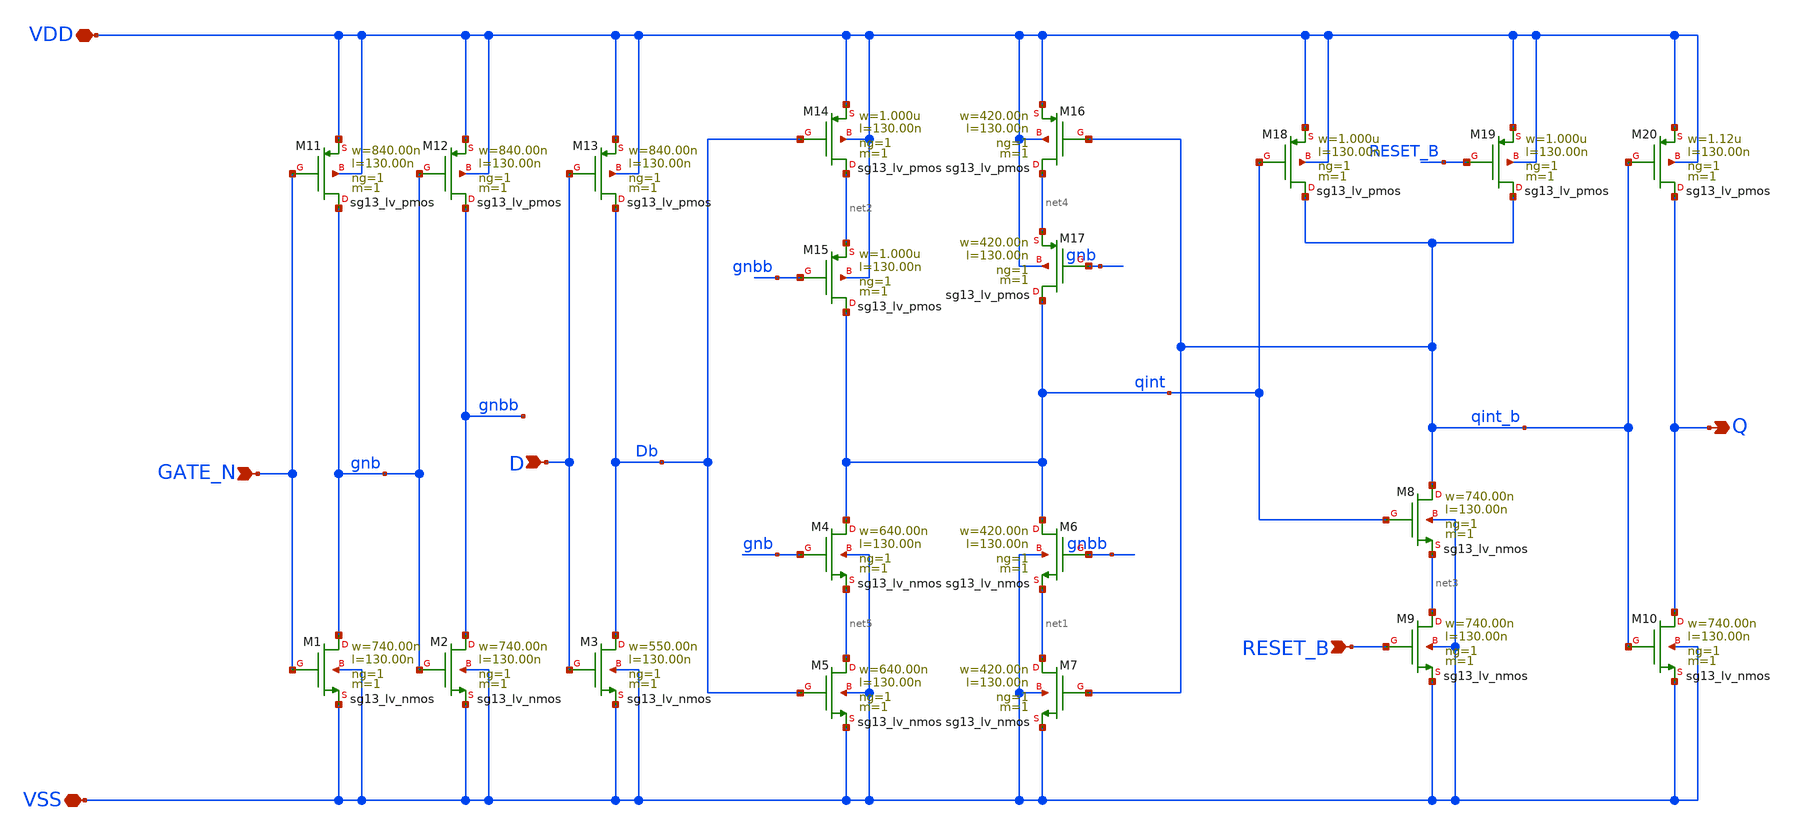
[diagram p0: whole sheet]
** sch_path: ihp-sg13g2/libs.tech/xschem/sg13g2_stdcells/sg13g2_dllrq_1.sch
* Copyright 2023 IHP PDK Authors
* Licensed under the Apache License, Version 2.0 (the "License");
* you may not use this file except in compliance with the License.
* You may obtain a copy of the License at
* https://www.apache.org/licenses/LICENSE-2.0
* Unless required by applicable law or agreed to in writing, software
* distributed under the License is distributed on an "AS IS" BASIS,
* WITHOUT WARRANTIES OR CONDITIONS OF ANY KIND, either express or implied.
* See the License for the specific language governing permissions and
* limitations under the License.
**.subckt sg13g2_dllrq_1 D GATE_N RESET_B Q VDD VSS
*.ipin D
*.ipin GATE_N
*.ipin RESET_B
*.opin Q
*.iopin VDD
*.iopin VSS
XM1 gnb GATE_N VSS VSS sg13_lv_nmos w=740.00n l=130.00n ng=1 m=1 mm_ok=1
XM2 gnbb gnb VSS VSS sg13_lv_nmos w=740.00n l=130.00n ng=1 m=1 mm_ok=1
XM3 Db D VSS VSS sg13_lv_nmos w=550.00n l=130.00n ng=1 m=1 mm_ok=1
XM4 qint gnb net5 VSS sg13_lv_nmos w=640.00n l=130.00n ng=1 m=1 mm_ok=1
XM5 net5 Db VSS VSS sg13_lv_nmos w=640.00n l=130.00n ng=1 m=1 mm_ok=1
XM6 qint gnbb net1 VSS sg13_lv_nmos w=420.00n l=130.00n ng=1 m=1 mm_ok=1
XM7 net1 qint_b VSS VSS sg13_lv_nmos w=420.00n l=130.00n ng=1 m=1 mm_ok=1
XM8 qint_b qint net3 VSS sg13_lv_nmos w=740.00n l=130.00n ng=1 m=1 mm_ok=1
XM9 net3 RESET_B VSS VSS sg13_lv_nmos w=740.00n l=130.00n ng=1 m=1 mm_ok=1
XM10 Q qint_b VSS VSS sg13_lv_nmos w=740.00n l=130.00n ng=1 m=1 mm_ok=1
XM11 gnb GATE_N VDD VDD sg13_lv_pmos w=840.00n l=130.00n ng=1 m=1 mm_ok=1
XM12 gnbb gnb VDD VDD sg13_lv_pmos w=840.00n l=130.00n ng=1 m=1 mm_ok=1
XM13 Db D VDD VDD sg13_lv_pmos w=840.00n l=130.00n ng=1 m=1 mm_ok=1
XM14 net2 Db VDD VDD sg13_lv_pmos w=1.000u l=130.00n ng=1 m=1 mm_ok=1
XM15 qint gnbb net2 VDD sg13_lv_pmos w=1.000u l=130.00n ng=1 m=1 mm_ok=1
XM16 net4 qint_b VDD VDD sg13_lv_pmos w=420.00n l=130.00n ng=1 m=1 mm_ok=1
XM17 qint gnb net4 VDD sg13_lv_pmos w=420.00n l=130.00n ng=1 m=1 mm_ok=1
XM18 qint_b qint VDD VDD sg13_lv_pmos w=1.000u l=130.00n ng=1 m=1 mm_ok=1
XM19 qint_b RESET_B VDD VDD sg13_lv_pmos w=1.000u l=130.00n ng=1 m=1 mm_ok=1
XM20 Q qint_b VDD VDD sg13_lv_pmos w=1.12u l=130.00n ng=1 m=1 mm_ok=1
**.ends
.end
